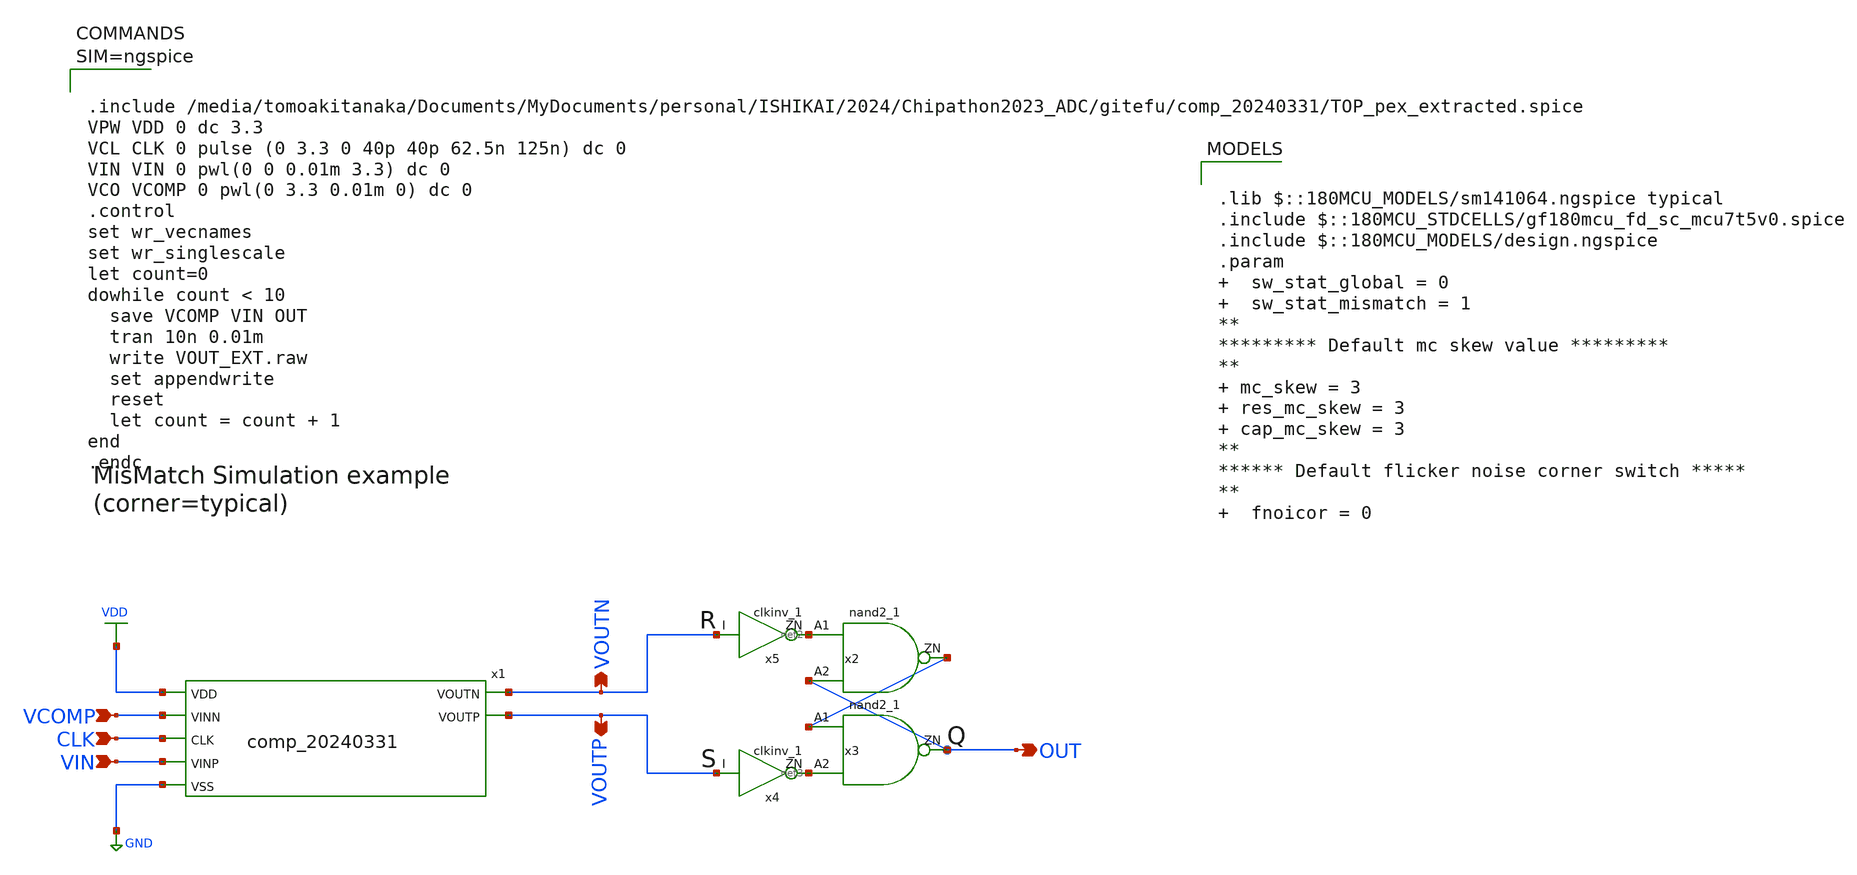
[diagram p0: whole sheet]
** sch_path: gitefu/tb/bench_mm.sch
**.subckt bench_mm VOUTN VOUTP VCOMP VIN CLK OUT
*.opin VOUTN
*.opin VOUTP
*.ipin VCOMP
*.ipin VIN
*.ipin CLK
*.opin OUT
x1 VDD CLK VOUTP VOUTN VIN VCOMP GND TOP
x2 net2 OUT net1 VDD VDD 0 0 gf180mcu_fd_sc_mcu7t5v0__nand2_1
x3 net1 net3 OUT VDD VDD 0 0 gf180mcu_fd_sc_mcu7t5v0__nand2_1
x4 VOUTP net3 VDD VDD 0 0 gf180mcu_fd_sc_mcu7t5v0__clkinv_1
x5 VOUTN net2 VDD VDD 0 0 gf180mcu_fd_sc_mcu7t5v0__clkinv_1
**** begin user architecture code



.include /media/tomoakitanaka/Documents/MyDocuments/personal/ISHIKAI/2024/Chipathon2023_ADC/gitefu/comp_20240331/TOP_pex_extracted.spice
VPW VDD 0 dc 3.3
VCL CLK 0 pulse (0 3.3 0 40p 40p 62.5n 125n) dc 0
VIN VIN 0 pwl(0 0 0.01m 3.3) dc 0
VCO VCOMP 0 pwl(0 3.3 0.01m 0) dc 0
.control
set wr_vecnames
set wr_singlescale
let count=0
dowhile count < 10
  save VCOMP VIN OUT
  tran 10n 0.01m
  write VOUT_EXT.raw
  set appendwrite
  reset
  let count = count + 1
end
.endc




.lib $::180MCU_MODELS/sm141064.ngspice typical
.include $::180MCU_STDCELLS/gf180mcu_fd_sc_mcu7t5v0.spice
.include $::180MCU_MODELS/design.ngspice
.param   sw_stat_global = 0   sw_stat_mismatch = 1
**
********* Default mc skew value *********
**  mc_skew = 3  res_mc_skew = 3  cap_mc_skew = 3
**
****** Default flicker noise corner switch *****
**   fnoicor = 0

**** end user architecture code
**.ends
.GLOBAL VDD
.GLOBAL GND
.end
